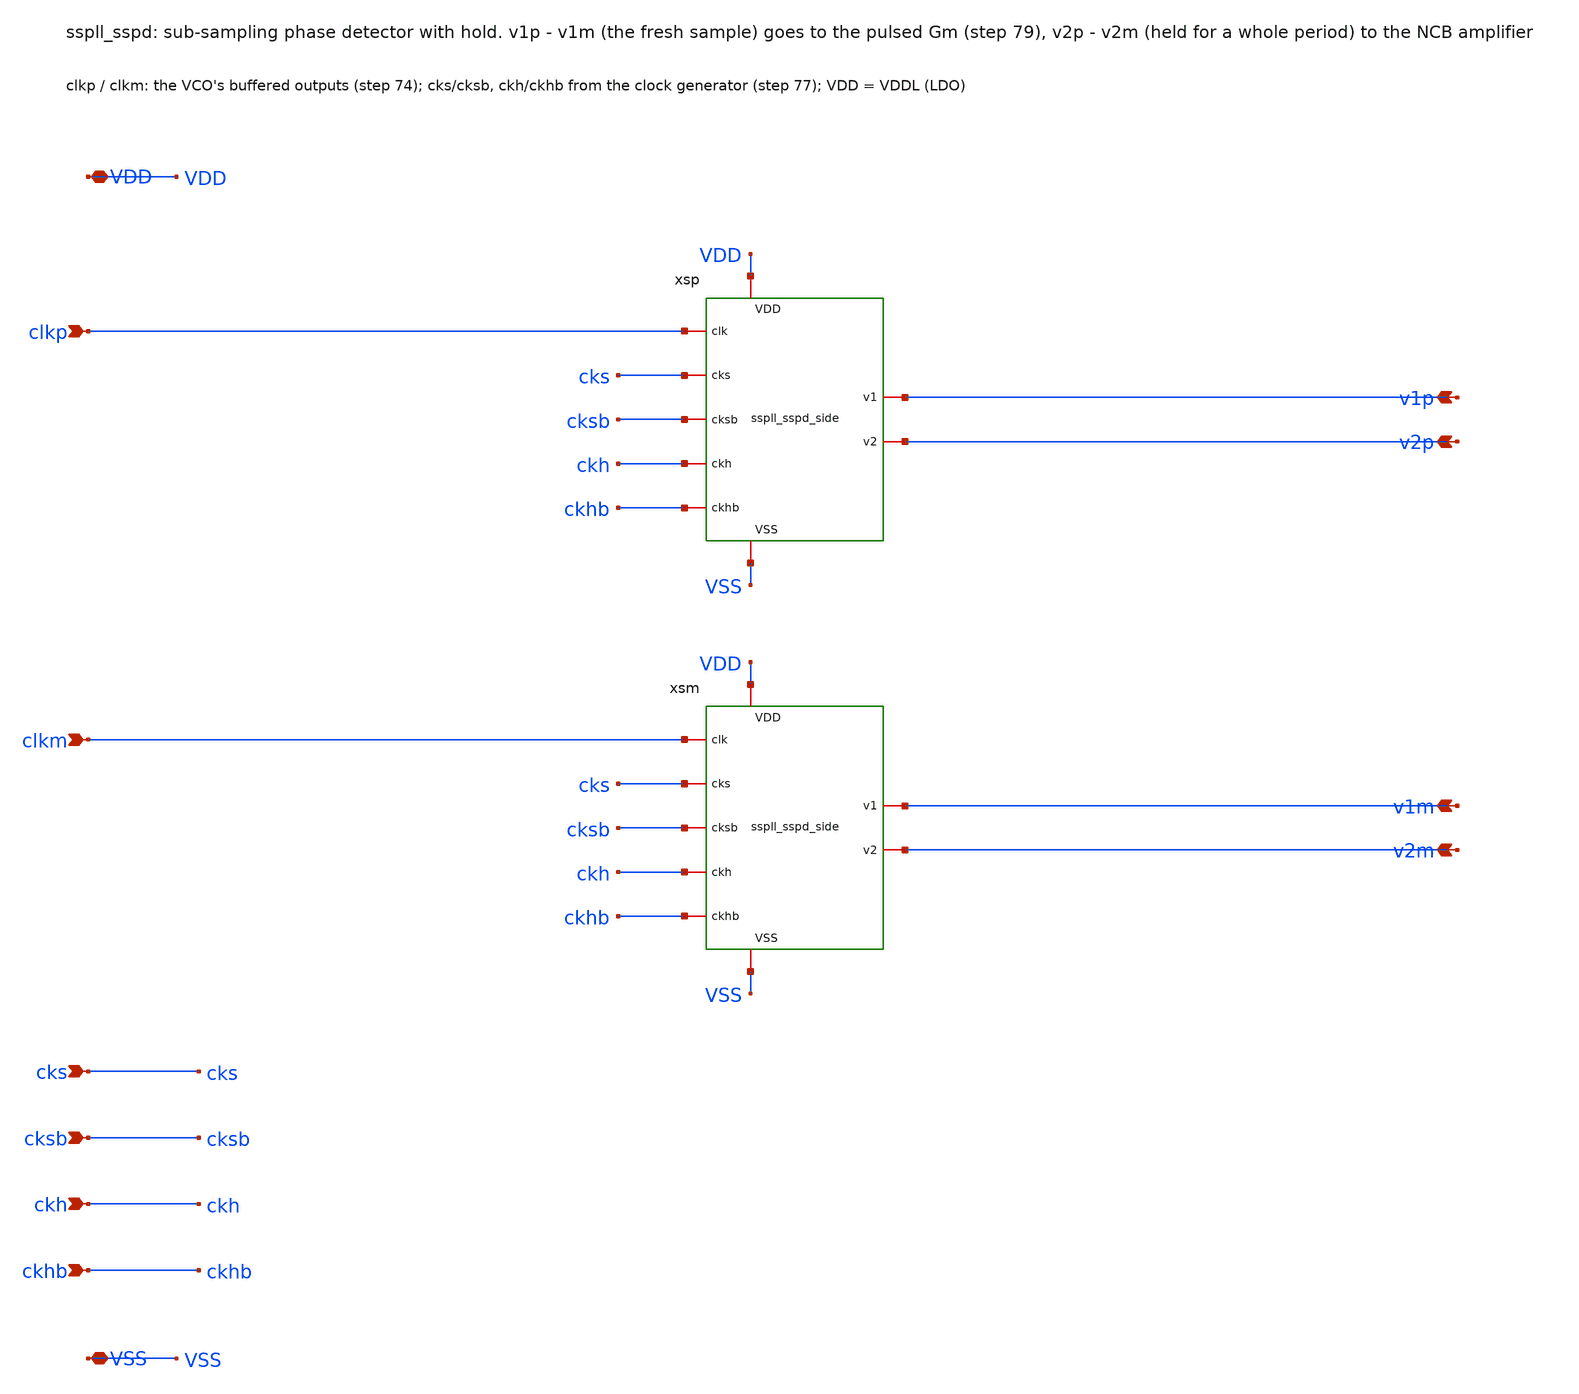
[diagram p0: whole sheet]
** sch_path: xschem/sspd/sspll_sspd.sch
**.subckt sspll_sspd clkp clkm v1p v2p v1m v2m cks cksb ckh ckhb VDD VSS
*.ipin clkp
*.ipin clkm
*.opin v1p
*.opin v2p
*.opin v1m
*.opin v2m
*.ipin cks
*.ipin cksb
*.ipin ckh
*.ipin ckhb
*.iopin VDD
*.iopin VSS
xsp clkp cks cksb ckh ckhb v1p v2p VDD VSS sspll_sspd_side
xsm clkm cks cksb ckh ckhb v1m v2m VDD VSS sspll_sspd_side
**.ends
.end
